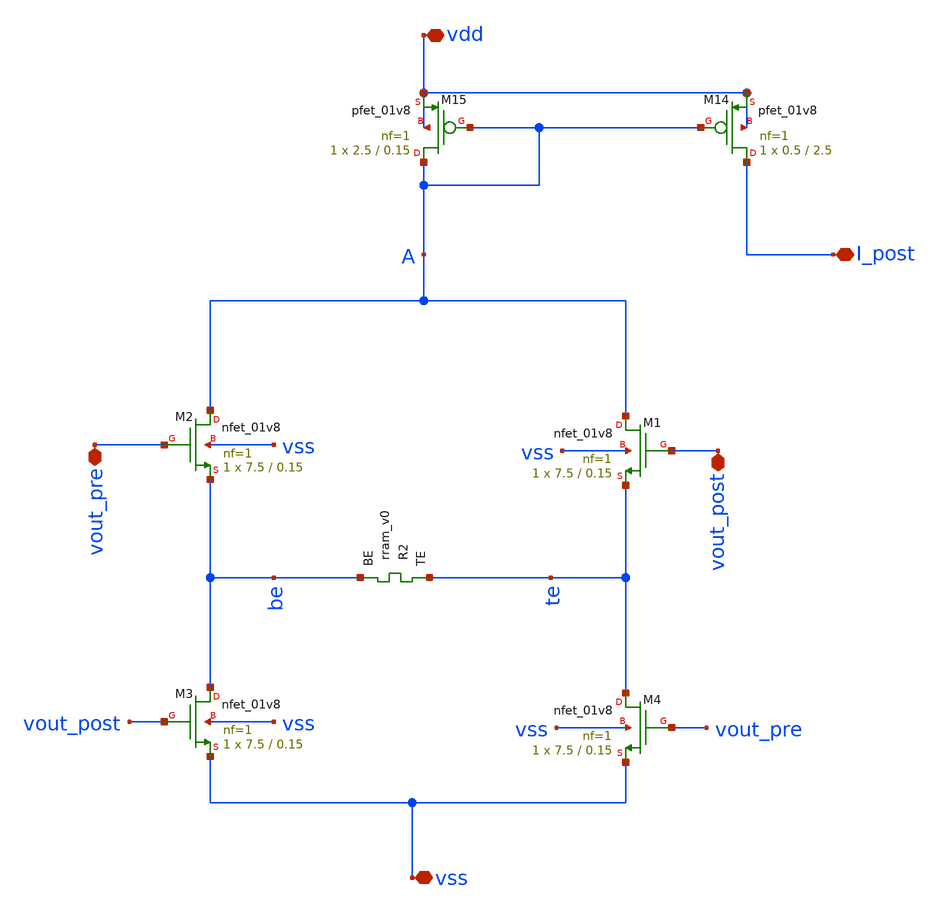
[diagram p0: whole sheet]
** sch_path: Synapse/stdp.sch
**.subckt stdp vdd vss vout_post vout_pre I_post
*.iopin vdd
*.iopin vss
*.iopin vout_post
*.iopin vout_pre
*.iopin I_post
XM2 A vout_pre be vss sky130_fd_pr__nfet_01v8 L=0.15 W=7.5 nf=1 ad='int((nf+1)/2) * W/nf * 0.29' as='int((nf+2)/2) * W/nf * 0.29'
+ pd='2*int((nf+1)/2) * (W/nf + 0.29)' ps='2*int((nf+2)/2) * (W/nf + 0.29)' nrd='0.29 / W' nrs='0.29 / W'
+ sa=0 sb=0 sd=0 mult=1 m=1
XM3 be vout_post vss vss sky130_fd_pr__nfet_01v8 L=0.15 W=7.5 nf=1 ad='int((nf+1)/2) * W/nf * 0.29' as='int((nf+2)/2) * W/nf * 0.29'
+ pd='2*int((nf+1)/2) * (W/nf + 0.29)' ps='2*int((nf+2)/2) * (W/nf + 0.29)' nrd='0.29 / W' nrs='0.29 / W'
+ sa=0 sb=0 sd=0 mult=1 m=1
XM1 A vout_post te vss sky130_fd_pr__nfet_01v8 L=0.15 W=7.5 nf=1 ad='int((nf+1)/2) * W/nf * 0.29' as='int((nf+2)/2) * W/nf * 0.29'
+ pd='2*int((nf+1)/2) * (W/nf + 0.29)' ps='2*int((nf+2)/2) * (W/nf + 0.29)' nrd='0.29 / W' nrs='0.29 / W'
+ sa=0 sb=0 sd=0 mult=1 m=1
XM4 te vout_pre vss vss sky130_fd_pr__nfet_01v8 L=0.15 W=7.5 nf=1 ad='int((nf+1)/2) * W/nf * 0.29' as='int((nf+2)/2) * W/nf * 0.29'
+ pd='2*int((nf+1)/2) * (W/nf + 0.29)' ps='2*int((nf+2)/2) * (W/nf + 0.29)' nrd='0.29 / W' nrs='0.29 / W'
+ sa=0 sb=0 sd=0 mult=1 m=1
XR2 te be rram_v0
XM14 I_post A vdd vdd sky130_fd_pr__pfet_01v8 L=2.5 W=0.5 nf=1 ad='int((nf+1)/2) * W/nf * 0.29' as='int((nf+2)/2) * W/nf * 0.29'
+ pd='2*int((nf+1)/2) * (W/nf + 0.29)' ps='2*int((nf+2)/2) * (W/nf + 0.29)' nrd='0.29 / W' nrs='0.29 / W'
+ sa=0 sb=0 sd=0 mult=1 m=1
XM15 A A vdd vdd sky130_fd_pr__pfet_01v8 L=0.15 W=2.5 nf=1 ad='int((nf+1)/2) * W/nf * 0.29' as='int((nf+2)/2) * W/nf * 0.29'
+ pd='2*int((nf+1)/2) * (W/nf + 0.29)' ps='2*int((nf+2)/2) * (W/nf + 0.29)' nrd='0.29 / W' nrs='0.29 / W'
+ sa=0 sb=0 sd=0 mult=1 m=1
**.ends
.end
